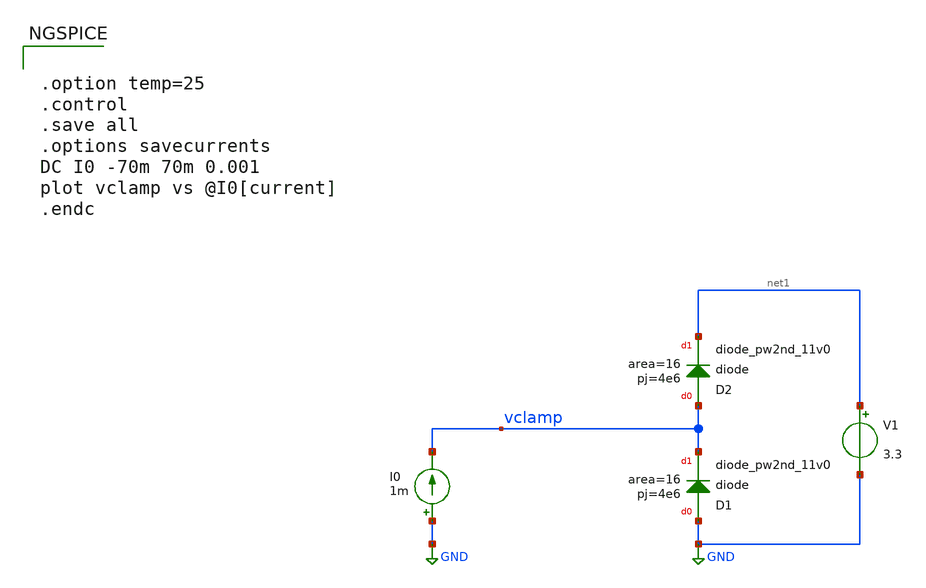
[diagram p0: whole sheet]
** sch_path: images/foss-asic-tools/addons/examples/open-pmic/characterization/N_diode_test.sch
**.subckt N_diode_test
I0 GND vclamp 1m
V1 net1 GND 3.3
XD2 vclamp net1 sky130_fd_pr__diode_pw2nd_11v0 area=16 pj=4e6
XD1 GND vclamp sky130_fd_pr__diode_pw2nd_11v0 area=16 pj=4e6
**** begin user architecture code


.option temp=25
.control
.save all
.options savecurrents
DC I0 -70m 70m 0.001
plot vclamp vs @I0[current]
.endc



.include $::SKYWATER_MODELS/cells/nfet_01v8/sky130_fd_pr__nfet_01v8__tt.corner.spice
.include $::SKYWATER_MODELS/cells/nfet_01v8_lvt/sky130_fd_pr__nfet_01v8_lvt__tt.corner.spice
.include $::SKYWATER_MODELS/cells/pfet_01v8/sky130_fd_pr__pfet_01v8__tt.corner.spice
.include $::SKYWATER_MODELS/cells/nfet_03v3_nvt/sky130_fd_pr__nfet_03v3_nvt__tt.corner.spice
.include $::SKYWATER_MODELS/cells/nfet_05v0_nvt/sky130_fd_pr__nfet_05v0_nvt__tt.corner.spice
.include $::SKYWATER_MODELS/cells/esd_nfet_01v8/sky130_fd_pr__esd_nfet_01v8__tt.corner.spice
.include $::SKYWATER_MODELS/cells/pfet_01v8_lvt/sky130_fd_pr__pfet_01v8_lvt__tt.corner.spice
.include $::SKYWATER_MODELS/cells/pfet_01v8_hvt/sky130_fd_pr__pfet_01v8_hvt__tt.corner.spice
.include $::SKYWATER_MODELS/cells/esd_pfet_g5v0d10v5/sky130_fd_pr__esd_pfet_g5v0d10v5__tt.corner.spice
.include $::SKYWATER_MODELS/cells/pfet_g5v0d10v5/sky130_fd_pr__pfet_g5v0d10v5__tt.corner.spice
.include $::SKYWATER_MODELS/cells/pfet_g5v0d16v0/sky130_fd_pr__pfet_g5v0d16v0__tt.corner.spice
.include $::SKYWATER_MODELS/cells/nfet_g5v0d10v5/sky130_fd_pr__nfet_g5v0d10v5__tt.corner.spice
.include $::SKYWATER_MODELS/cells/nfet_g5v0d16v0/sky130_fd_pr__nfet_g5v0d16v0__tt_discrete.corner.spice
.include $::SKYWATER_MODELS/cells/esd_nfet_g5v0d10v5/sky130_fd_pr__esd_nfet_g5v0d10v5__tt.corner.spice
.include $::SKYWATER_MODELS/models/corners/tt/nonfet.spice
* Mismatch parameters
.include $::SKYWATER_MODELS/cells/nfet_01v8/sky130_fd_pr__nfet_01v8__mismatch.corner.spice
.include $::SKYWATER_MODELS/cells/pfet_01v8/sky130_fd_pr__pfet_01v8__mismatch.corner.spice
.include $::SKYWATER_MODELS/cells/nfet_01v8_lvt/sky130_fd_pr__nfet_01v8_lvt__mismatch.corner.spice
.include $::SKYWATER_MODELS/cells/pfet_01v8_lvt/sky130_fd_pr__pfet_01v8_lvt__mismatch.corner.spice
.include $::SKYWATER_MODELS/cells/pfet_01v8_hvt/sky130_fd_pr__pfet_01v8_hvt__mismatch.corner.spice
.include $::SKYWATER_MODELS/cells/nfet_g5v0d10v5/sky130_fd_pr__nfet_g5v0d10v5__mismatch.corner.spice
.include $::SKYWATER_MODELS/cells/pfet_g5v0d10v5/sky130_fd_pr__pfet_g5v0d10v5__mismatch.corner.spice
.include $::SKYWATER_MODELS/cells/nfet_05v0_nvt/sky130_fd_pr__nfet_05v0_nvt__mismatch.corner.spice
.include $::SKYWATER_MODELS/cells/nfet_03v3_nvt/sky130_fd_pr__nfet_03v3_nvt__mismatch.corner.spice
* Resistor$::SKYWATER_MODELS/Capacitor
.include $::SKYWATER_MODELS/models/r+c/res_typical__cap_typical.spice
.include $::SKYWATER_MODELS/models/r+c/res_typical__cap_typical__lin.spice
* Special cells
.include $::SKYWATER_MODELS/models/corners/tt/specialized_cells.spice
* All models
.include $::SKYWATER_MODELS/models/all.spice
* Corner
.include $::SKYWATER_MODELS/models/corners/tt/rf.spice
.include $::SKYWATER_MODELS/models/sky130_fd_pr__model__diode_pd2nw_11v0.model.spice
.include $::SKYWATER_MODELS/models/sky130_fd_pr__model__diode_pw2nd_11v0.model.spice


**** end user architecture code
**.ends
.GLOBAL GND
.end
